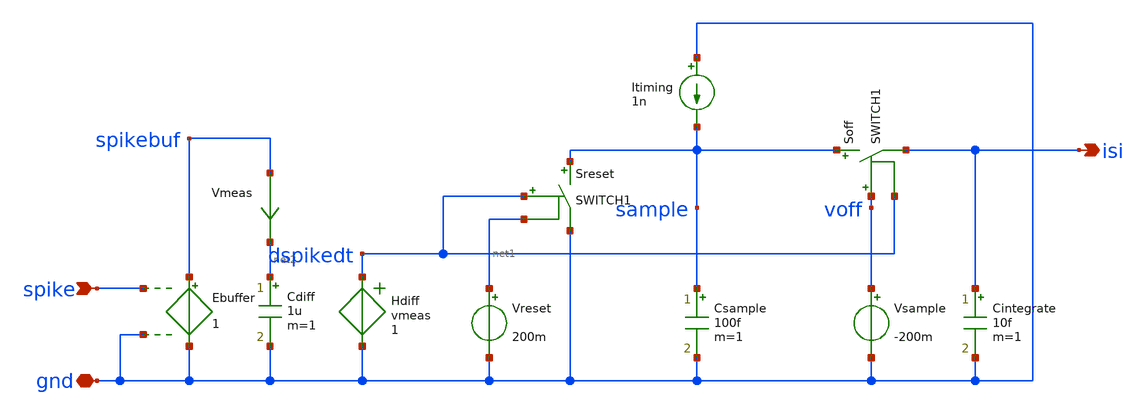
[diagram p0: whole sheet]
** sch_path: playground/InterServicesIntelligence.sch
**.subckt InterServicesIntelligence gnd spike isi
*.iopin gnd
*.ipin spike
*.opin isi
Csample sample gnd 100f m=1
Itiming gnd sample 1n
Sreset sample gnd dspikedt net1 SWITCH1
Cintegrate isi gnd 10f m=1
Vreset net1 gnd 200m
Soff sample isi voff dspikedt SWITCH1
Vsample voff gnd -200m
Ebuffer spikebuf gnd spike gnd 1
Cdiff net2 gnd 1u m=1
Vmeas spikebuf net2 0
.save i(vmeas)
Hdiff dspikedt gnd vmeas 1
**.ends
.end
